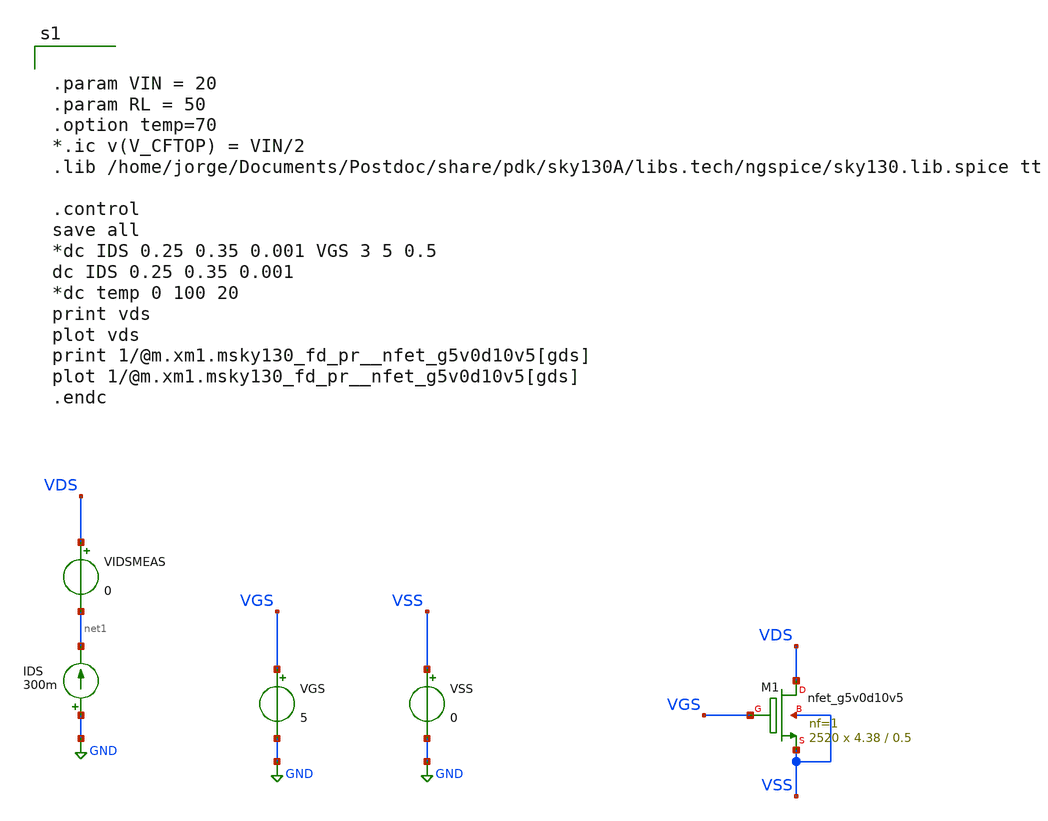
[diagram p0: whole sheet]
** sch_path: xschem/dev_switches/NMOS_allfingers_RONcalc_v2p2_20220626.sch
**.subckt NMOS_allfingers_RONcalc_v2p2_20220626
XM1 VDS VGS VSS VSS sky130_fd_pr__nfet_g5v0d10v5 L=0.5 W=4.38 nf=1 ad='int((nf+1)/2) * W/nf * 0.29' as='int((nf+2)/2) * W/nf * 0.29'
+ pd='2*int((nf+1)/2) * (W/nf + 0.29)' ps='2*int((nf+2)/2) * (W/nf + 0.29)' nrd='0.29 / W' nrs='0.29 / W'
+ sa=0 sb=0 sd=0 mult=2520 m=2520
VGS VGS GND 5
VSS VSS GND 0
IDS GND net1 300m
VIDSMEAS VDS net1 0
**** begin user architecture code


.param VIN = 20
.param RL = 50
.option temp=70
*.ic v(V_CFTOP) = VIN/2
.lib /home/jorge/Documents/Postdoc/share/pdk/sky130A/libs.tech/ngspice/sky130.lib.spice tt

.control
save all
*dc IDS 0.25 0.35 0.001 VGS 3 5 0.5
dc IDS 0.25 0.35 0.001
*dc temp 0 100 20
print vds
plot vds
print 1/@m.xm1.msky130_fd_pr__nfet_g5v0d10v5[gds]
plot 1/@m.xm1.msky130_fd_pr__nfet_g5v0d10v5[gds]
.endc



**** end user architecture code
**.ends
.GLOBAL GND
.end
